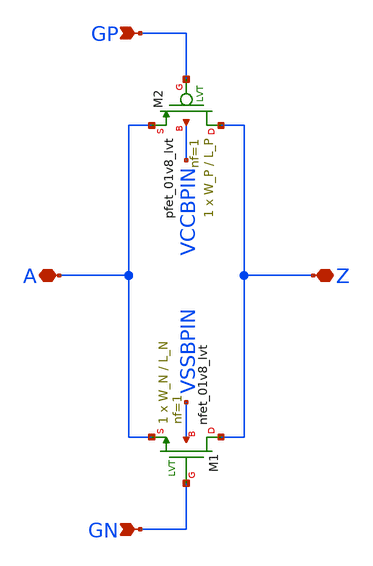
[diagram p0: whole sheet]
** sch_path: pdks/sky130A-1.0.227.01/libs.tech/xschem/sky130_tests/passgate_nlvt.sch
* Copyright 2021 Stefan Frederik Schippers
* Licensed under the Apache License, Version 2.0 (the "License");
* you may not use this file except in compliance with the License.
* You may obtain a copy of the License at
* https://www.apache.org/licenses/LICENSE-2.0
* Unless required by applicable law or agreed to in writing, software
* distributed under the License is distributed on an "AS IS" BASIS,
* WITHOUT WARRANTIES OR CONDITIONS OF ANY KIND, either express or implied.
* See the License for the specific language governing permissions and
* limitations under the License.
**.subckt passgate_nlvt A Z GP GN
*.iopin A
*.iopin Z
*.ipin GP
*.ipin GN
XM1 Z GN A VSSBPIN sky130_fd_pr__nfet_01v8_lvt L=L_N W=W_N nf=1 ad='int((nf+1)/2) * W/nf * 0.29' as='int((nf+2)/2) * W/nf * 0.29'
+ pd='2*int((nf+1)/2) * (W/nf + 0.29)' ps='2*int((nf+2)/2) * (W/nf + 0.29)' nrd='0.29 / W' nrs='0.29 / W'
+ sa=0 sb=0 sd=0 mult=1 m=1
XM2 Z GP A VCCBPIN sky130_fd_pr__pfet_01v8_lvt L=L_P W=W_P nf=1 ad='int((nf+1)/2) * W/nf * 0.29' as='int((nf+2)/2) * W/nf * 0.29'
+ pd='2*int((nf+1)/2) * (W/nf + 0.29)' ps='2*int((nf+2)/2) * (W/nf + 0.29)' nrd='0.29 / W' nrs='0.29 / W'
+ sa=0 sb=0 sd=0 mult=1 m=1
**** begin user architecture code

.lib $::SKYWATER_MODELS/sky130.lib.spice tt

**** end user architecture code
**.ends
.end
